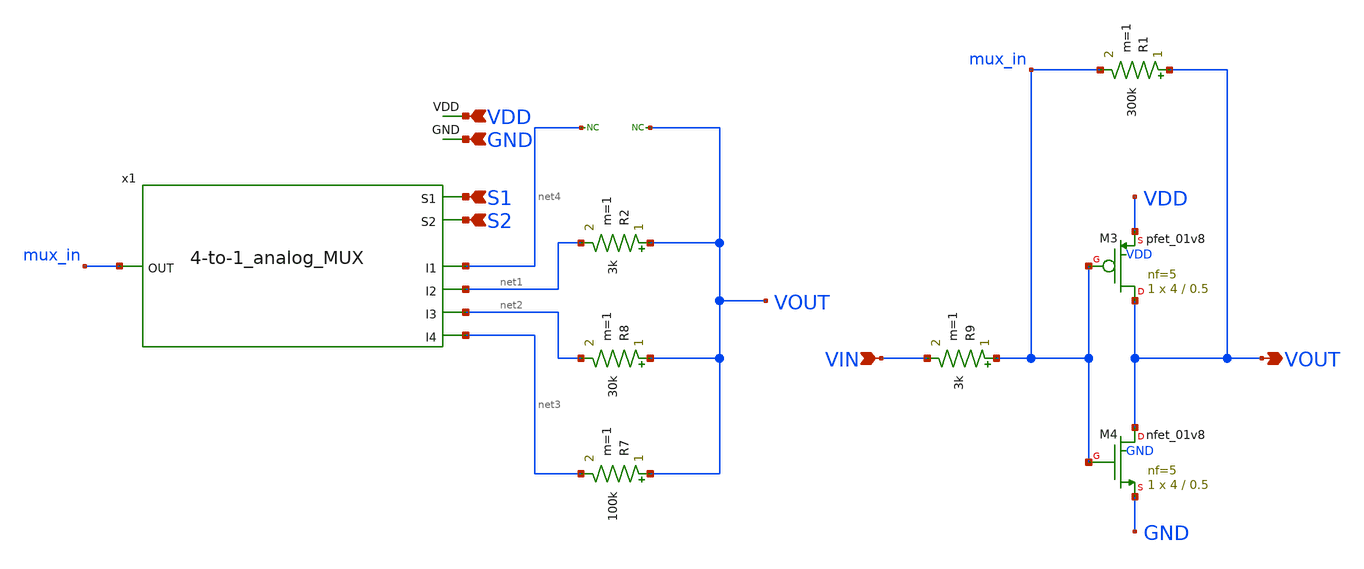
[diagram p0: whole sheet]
** sch_path: xschem/mixedsignal.sch
**.subckt mixedsignal VOUT VIN S1 S2 VDD GND
*.opin VOUT
*.ipin VIN
*.ipin S1
*.ipin S2
*.ipin VDD
*.ipin GND
R1 VOUT mux_in 300k m=1
XM3 VOUT mux_in VDD VDD sky130_fd_pr__pfet_01v8 L=0.5 W=4 nf=5 ad='int((nf+1)/2) * W/nf * 0.29' as='int((nf+2)/2) * W/nf * 0.29'
+ pd='2*int((nf+1)/2) * (W/nf + 0.29)' ps='2*int((nf+2)/2) * (W/nf + 0.29)' nrd='0.29 / W' nrs='0.29 / W'
+ sa=0 sb=0 sd=0 mult=1 m=1
XM4 VOUT mux_in GND GND sky130_fd_pr__nfet_01v8 L=0.5 W=4 nf=5 ad='int((nf+1)/2) * W/nf * 0.29' as='int((nf+2)/2) * W/nf * 0.29'
+ pd='2*int((nf+1)/2) * (W/nf + 0.29)' ps='2*int((nf+2)/2) * (W/nf + 0.29)' nrd='0.29 / W' nrs='0.29 / W'
+ sa=0 sb=0 sd=0 mult=1 m=1
R7 VOUT net3 100k m=1
x1 S1 S2 VDD GND net4 net1 mux_in net2 net3 4-to-1_analog_MUX
R8 VOUT net2 30k m=1
R9 mux_in VIN 3k m=1
* noconn VOUT
* noconn #net4
R2 VOUT net1 3k m=1
**.ends

* expanding   symbol:  4-to-1_analog_MUX.sym # of pins=9
** sym_path: xschem/4-to-1_analog_MUX.sym
** sch_path: xschem/4-to-1_analog_MUX.sch
.subckt 4-to-1_analog_MUX S1 S2 VDD GND I1 I2 OUT I3 I4
*.ipin I1
*.ipin I2
*.ipin I3
*.ipin I4
*.opin OUT
*.ipin S1
*.ipin S2
*.ipin VDD
*.ipin GND
x1 S1 S1bar GND VDD Inverter
x2 S2 S2bar GND VDD Inverter
XM9 net1 S2 OUT VDD sky130_fd_pr__pfet_01v8 L=0.5 W=1 nf=1 ad='int((nf+1)/2) * W/nf * 0.29' as='int((nf+2)/2) * W/nf * 0.29'
+ pd='2*int((nf+1)/2) * (W/nf + 0.29)' ps='2*int((nf+2)/2) * (W/nf + 0.29)' nrd='0.29 / W' nrs='0.29 / W'
+ sa=0 sb=0 sd=0 mult=1 m=1
XM1 I1 S1 net1 VDD sky130_fd_pr__pfet_01v8 L=0.5 W=1 nf=1 ad='int((nf+1)/2) * W/nf * 0.29' as='int((nf+2)/2) * W/nf * 0.29'
+ pd='2*int((nf+1)/2) * (W/nf + 0.29)' ps='2*int((nf+2)/2) * (W/nf + 0.29)' nrd='0.29 / W' nrs='0.29 / W'
+ sa=0 sb=0 sd=0 mult=1 m=1
XM2 I3 S1bar net1 VDD sky130_fd_pr__pfet_01v8 L=0.5 W=1 nf=1 ad='int((nf+1)/2) * W/nf * 0.29' as='int((nf+2)/2) * W/nf * 0.29'
+ pd='2*int((nf+1)/2) * (W/nf + 0.29)' ps='2*int((nf+2)/2) * (W/nf + 0.29)' nrd='0.29 / W' nrs='0.29 / W'
+ sa=0 sb=0 sd=0 mult=1 m=1
XM5 I2 S1 net2 VDD sky130_fd_pr__pfet_01v8 L=0.5 W=1 nf=1 ad='int((nf+1)/2) * W/nf * 0.29' as='int((nf+2)/2) * W/nf * 0.29'
+ pd='2*int((nf+1)/2) * (W/nf + 0.29)' ps='2*int((nf+2)/2) * (W/nf + 0.29)' nrd='0.29 / W' nrs='0.29 / W'
+ sa=0 sb=0 sd=0 mult=1 m=1
XM7 I4 S1bar net2 VDD sky130_fd_pr__pfet_01v8 L=0.5 W=1 nf=1 ad='int((nf+1)/2) * W/nf * 0.29' as='int((nf+2)/2) * W/nf * 0.29'
+ pd='2*int((nf+1)/2) * (W/nf + 0.29)' ps='2*int((nf+2)/2) * (W/nf + 0.29)' nrd='0.29 / W' nrs='0.29 / W'
+ sa=0 sb=0 sd=0 mult=1 m=1
XM11 net2 S2bar OUT VDD sky130_fd_pr__pfet_01v8 L=0.5 W=1 nf=1 ad='int((nf+1)/2) * W/nf * 0.29' as='int((nf+2)/2) * W/nf * 0.29'
+ pd='2*int((nf+1)/2) * (W/nf + 0.29)' ps='2*int((nf+2)/2) * (W/nf + 0.29)' nrd='0.29 / W' nrs='0.29 / W'
+ sa=0 sb=0 sd=0 mult=1 m=1
XM3 I1 S1bar net1 GND sky130_fd_pr__nfet_01v8 L=1 W=1 nf=1 ad='int((nf+1)/2) * W/nf * 0.29' as='int((nf+2)/2) * W/nf * 0.29'
+ pd='2*int((nf+1)/2) * (W/nf + 0.29)' ps='2*int((nf+2)/2) * (W/nf + 0.29)' nrd='0.29 / W' nrs='0.29 / W'
+ sa=0 sb=0 sd=0 mult=1 m=1
XM4 I3 S1 net1 GND sky130_fd_pr__nfet_01v8 L=1 W=1 nf=1 ad='int((nf+1)/2) * W/nf * 0.29' as='int((nf+2)/2) * W/nf * 0.29'
+ pd='2*int((nf+1)/2) * (W/nf + 0.29)' ps='2*int((nf+2)/2) * (W/nf + 0.29)' nrd='0.29 / W' nrs='0.29 / W'
+ sa=0 sb=0 sd=0 mult=1 m=1
XM10 net1 S2bar OUT GND sky130_fd_pr__nfet_01v8 L=1 W=1 nf=1 ad='int((nf+1)/2) * W/nf * 0.29' as='int((nf+2)/2) * W/nf * 0.29'
+ pd='2*int((nf+1)/2) * (W/nf + 0.29)' ps='2*int((nf+2)/2) * (W/nf + 0.29)' nrd='0.29 / W' nrs='0.29 / W'
+ sa=0 sb=0 sd=0 mult=1 m=1
XM6 I2 S1bar net2 GND sky130_fd_pr__nfet_01v8 L=1 W=1 nf=1 ad='int((nf+1)/2) * W/nf * 0.29' as='int((nf+2)/2) * W/nf * 0.29'
+ pd='2*int((nf+1)/2) * (W/nf + 0.29)' ps='2*int((nf+2)/2) * (W/nf + 0.29)' nrd='0.29 / W' nrs='0.29 / W'
+ sa=0 sb=0 sd=0 mult=1 m=1
XM8 I4 S1 net2 GND sky130_fd_pr__nfet_01v8 L=1 W=1 nf=1 ad='int((nf+1)/2) * W/nf * 0.29' as='int((nf+2)/2) * W/nf * 0.29'
+ pd='2*int((nf+1)/2) * (W/nf + 0.29)' ps='2*int((nf+2)/2) * (W/nf + 0.29)' nrd='0.29 / W' nrs='0.29 / W'
+ sa=0 sb=0 sd=0 mult=1 m=1
XM12 net2 S2 OUT GND sky130_fd_pr__nfet_01v8 L=1 W=1 nf=1 ad='int((nf+1)/2) * W/nf * 0.29' as='int((nf+2)/2) * W/nf * 0.29'
+ pd='2*int((nf+1)/2) * (W/nf + 0.29)' ps='2*int((nf+2)/2) * (W/nf + 0.29)' nrd='0.29 / W' nrs='0.29 / W'
+ sa=0 sb=0 sd=0 mult=1 m=1
.ends


* expanding   symbol:  Inverter.sym # of pins=4
** sym_path: xschem/Inverter.sym
** sch_path: xschem/Inverter.sch
.subckt Inverter Vin Vout GND VDD
*.opin Vout
*.ipin Vin
*.ipin VDD
*.ipin GND
XM1 Vout Vin VDD VDD sky130_fd_pr__pfet_01v8 L=0.5 W=1 nf=1 ad='int((nf+1)/2) * W/nf * 0.29' as='int((nf+2)/2) * W/nf * 0.29'
+ pd='2*int((nf+1)/2) * (W/nf + 0.29)' ps='2*int((nf+2)/2) * (W/nf + 0.29)' nrd='0.29 / W' nrs='0.29 / W'
+ sa=0 sb=0 sd=0 mult=1 m=1
XM2 Vout Vin GND GND sky130_fd_pr__nfet_01v8 L=1 W=1 nf=1 ad='int((nf+1)/2) * W/nf * 0.29' as='int((nf+2)/2) * W/nf * 0.29'
+ pd='2*int((nf+1)/2) * (W/nf + 0.29)' ps='2*int((nf+2)/2) * (W/nf + 0.29)' nrd='0.29 / W' nrs='0.29 / W'
+ sa=0 sb=0 sd=0 mult=1 m=1
.ends

.end
